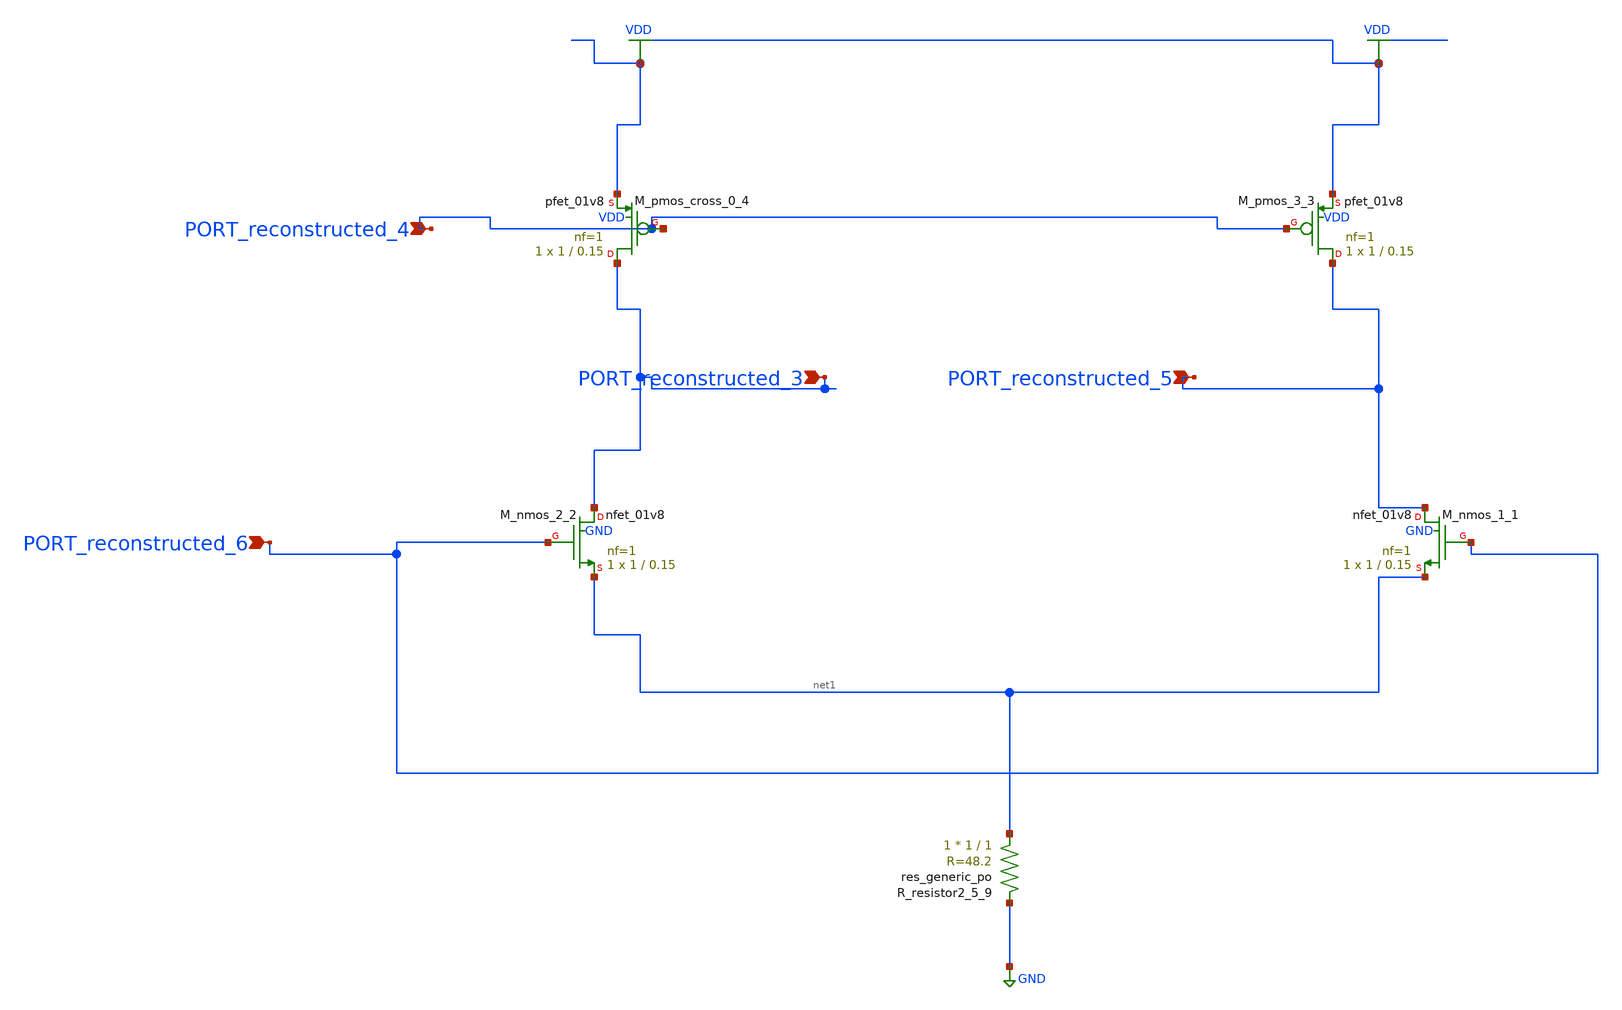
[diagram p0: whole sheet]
** sch_path: schematics/AMSNet/294.sch
**.subckt 294 PORT_reconstructed_4 PORT_reconstructed_5 PORT_reconstructed_3 PORT_reconstructed_6
*.ipin PORT_reconstructed_4
*.ipin PORT_reconstructed_5
*.ipin PORT_reconstructed_3
*.ipin PORT_reconstructed_6
XM_nmos_1_1 PORT_reconstructed_5 PORT_reconstructed_6 net1 GND sky130_fd_pr__nfet_01v8 L=0.15 W=1 nf=1
+ ad='int((1 + 1)/2) * 1 / 1 * 0.29' as='int((1 + 2)/2) * 1 / 1 * 0.29' pd='2*int((1 + 1)/2) * (1 / 1 + 0.29)'
+ ps='2*int((1 + 2)/2) * (1 / 1 + 0.29)' nrd='0.29 / 1 ' nrs='0.29 / 1 ' sa=0 sb=0 sd=0 mult=1 m=1
XM_nmos_2_2 PORT_reconstructed_3 PORT_reconstructed_6 net1 GND sky130_fd_pr__nfet_01v8 L=0.15 W=1 nf=1
+ ad='int((1 + 1)/2) * 1 / 1 * 0.29' as='int((1 + 2)/2) * 1 / 1 * 0.29' pd='2*int((1 + 1)/2) * (1 / 1 + 0.29)'
+ ps='2*int((1 + 2)/2) * (1 / 1 + 0.29)' nrd='0.29 / 1 ' nrs='0.29 / 1 ' sa=0 sb=0 sd=0 mult=1 m=1
XM_pmos_3_3 PORT_reconstructed_5 PORT_reconstructed_4 VDD VDD sky130_fd_pr__pfet_01v8 L=0.15 W=1 nf=1
+ ad='int((1 + 1)/2) * 1 / 1 * 0.29' as='int((1 + 2)/2) * 1 / 1 * 0.29' pd='2*int((1 + 1)/2) * (1 / 1 + 0.29)'
+ ps='2*int((1 + 2)/2) * (1 / 1 + 0.29)' nrd='0.29 / 1 ' nrs='0.29 / 1 ' sa=0 sb=0 sd=0 mult=1 m=1
XM_pmos_cross_0_4 PORT_reconstructed_3 PORT_reconstructed_4 VDD VDD sky130_fd_pr__pfet_01v8 L=0.15 W=1
+ nf=1 ad='int((1 + 1)/2) * 1 / 1 * 0.29' as='int((1 + 2)/2) * 1 / 1 * 0.29' pd='2*int((1 + 1)/2) * (1 / 1 + 0.29)'
+ ps='2*int((1 + 2)/2) * (1 / 1 + 0.29)' nrd='0.29 / 1 ' nrs='0.29 / 1 ' sa=0 sb=0 sd=0 mult=1 m=1
XR_resistor2_5_9 net1 GND sky130_fd_pr__res_generic_po W=1 L=1 m=1
**.ends
.GLOBAL GND
.GLOBAL VDD
.end
